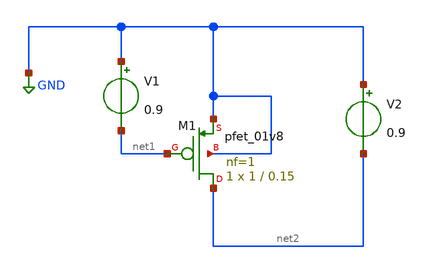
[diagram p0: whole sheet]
** sch_path: PMOS_Charac/pmos_gmid.sch
**.subckt pmos_gmid
V1 GND net1 0.9
V2 GND net2 0.9
XM1 net2 net1 GND GND sky130_fd_pr__pfet_01v8 L=0.15 W=1 nf=1 ad='int((nf+1)/2) * W/nf * 0.29' as='int((nf+2)/2) * W/nf * 0.29'
+ pd='2*int((nf+1)/2) * (W/nf + 0.29)' ps='2*int((nf+2)/2) * (W/nf + 0.29)' nrd='0.29 / W' nrs='0.29 / W'
+ sa=0 sb=0 sd=0 mult=1 m=1
**** begin user architecture code



.include init.txt
.include pmos_params.txt

.param length = 0.15
.param width = 1






**** end user architecture code
**.ends
.GLOBAL GND
.end
